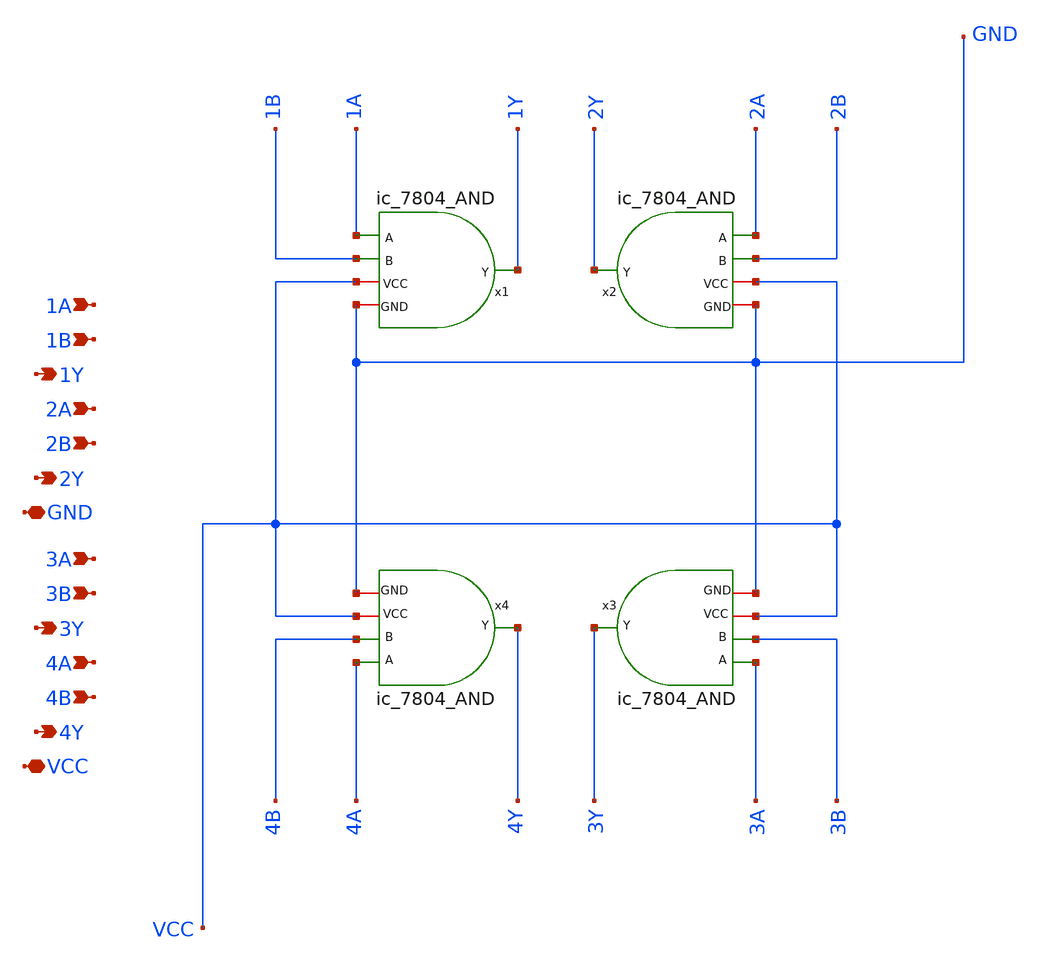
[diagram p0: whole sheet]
** sch_path: xschem/AND_IC_TopLevel.sch
**.subckt AND_IC_TopLevel 1A GND 1Y 1B 2A 2B 3A 3B 4A 4B 2Y 3Y 4Y VCC
*.ipin 1A
*.iopin GND
*.opin 1Y
*.ipin 1B
*.ipin 2A
*.ipin 2B
*.ipin 3A
*.ipin 3B
*.ipin 4A
*.ipin 4B
*.opin 2Y
*.opin 3Y
*.opin 4Y
*.iopin VCC
x1 1A 1B 1Y VCC GND ic_7804_AND
x2 2A 2B 2Y VCC GND ic_7804_AND
x3 3A 3B 3Y VCC GND ic_7804_AND
x4 4A 4B 4Y VCC GND ic_7804_AND
**.ends

* expanding   symbol:  ic_7804_AND.sym # of pins=5
** sym_path: xschem/ic_7804_AND.sym
** sch_path: xschem/ic_7804_AND.sch
.subckt ic_7804_AND A B Y VCC GND
*.ipin A
*.opin Y
*.ipin B
*.iopin VCC
*.iopin GND
XM2 net1 A VCC VCC sky130_fd_pr__pfet_01v8 L=0.15 W=2 nf=1 ad='int((nf+1)/2) * W/nf * 0.29' as='int((nf+2)/2) * W/nf * 0.29'
+ pd='2*int((nf+1)/2) * (W/nf + 0.29)' ps='2*int((nf+2)/2) * (W/nf + 0.29)' nrd='0.29 / W' nrs='0.29 / W'
+ sa=0 sb=0 sd=0 mult=1 m=1
XM3 net1 B VCC VCC sky130_fd_pr__pfet_01v8 L=0.15 W=2 nf=1 ad='int((nf+1)/2) * W/nf * 0.29' as='int((nf+2)/2) * W/nf * 0.29'
+ pd='2*int((nf+1)/2) * (W/nf + 0.29)' ps='2*int((nf+2)/2) * (W/nf + 0.29)' nrd='0.29 / W' nrs='0.29 / W'
+ sa=0 sb=0 sd=0 mult=1 m=1
XM5 Y net1 VCC VCC sky130_fd_pr__pfet_01v8 L=0.15 W=2 nf=1 ad='int((nf+1)/2) * W/nf * 0.29' as='int((nf+2)/2) * W/nf * 0.29'
+ pd='2*int((nf+1)/2) * (W/nf + 0.29)' ps='2*int((nf+2)/2) * (W/nf + 0.29)' nrd='0.29 / W' nrs='0.29 / W'
+ sa=0 sb=0 sd=0 mult=1 m=1
XM1 net1 A net2 GND sky130_fd_pr__nfet_01v8 L=0.15 W=1 nf=1 ad='int((nf+1)/2) * W/nf * 0.29' as='int((nf+2)/2) * W/nf * 0.29'
+ pd='2*int((nf+1)/2) * (W/nf + 0.29)' ps='2*int((nf+2)/2) * (W/nf + 0.29)' nrd='0.29 / W' nrs='0.29 / W'
+ sa=0 sb=0 sd=0 mult=1 m=1
XM4 net2 B GND GND sky130_fd_pr__nfet_01v8 L=0.15 W=1 nf=1 ad='int((nf+1)/2) * W/nf * 0.29' as='int((nf+2)/2) * W/nf * 0.29'
+ pd='2*int((nf+1)/2) * (W/nf + 0.29)' ps='2*int((nf+2)/2) * (W/nf + 0.29)' nrd='0.29 / W' nrs='0.29 / W'
+ sa=0 sb=0 sd=0 mult=1 m=1
XM6 Y net1 GND GND sky130_fd_pr__nfet_01v8 L=0.15 W=1 nf=1 ad='int((nf+1)/2) * W/nf * 0.29' as='int((nf+2)/2) * W/nf * 0.29'
+ pd='2*int((nf+1)/2) * (W/nf + 0.29)' ps='2*int((nf+2)/2) * (W/nf + 0.29)' nrd='0.29 / W' nrs='0.29 / W'
+ sa=0 sb=0 sd=0 mult=1 m=1
.ends

.end
